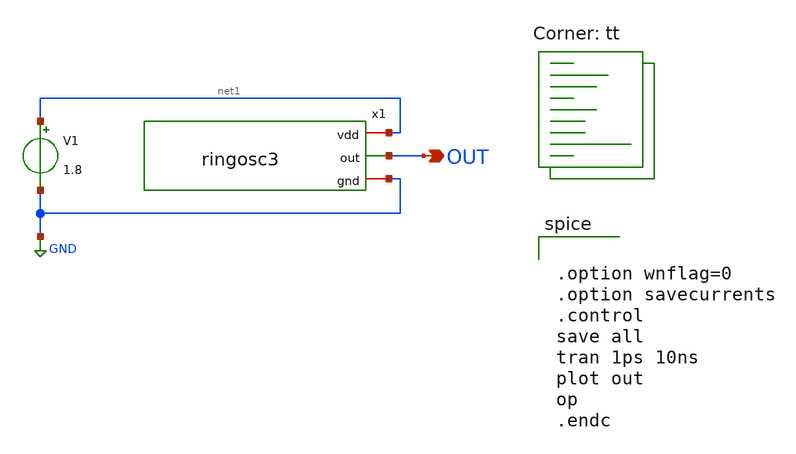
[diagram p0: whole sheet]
** sch_path: ring_oscillator/ringosc3_tb.sch
**.subckt ringosc3_tb OUT
*.opin OUT
V1 net1 GND 1.8
x1 net1 OUT GND ringosc3
**** begin user architecture code


.option wnflag=0
.option savecurrents
.control
save all
tran 1ps 10ns
plot out
op
.endc


.lib $::SKYWATER_MODELS/sky130.lib.spice tt
**** end user architecture code
**.ends
.GLOBAL GND
.end
